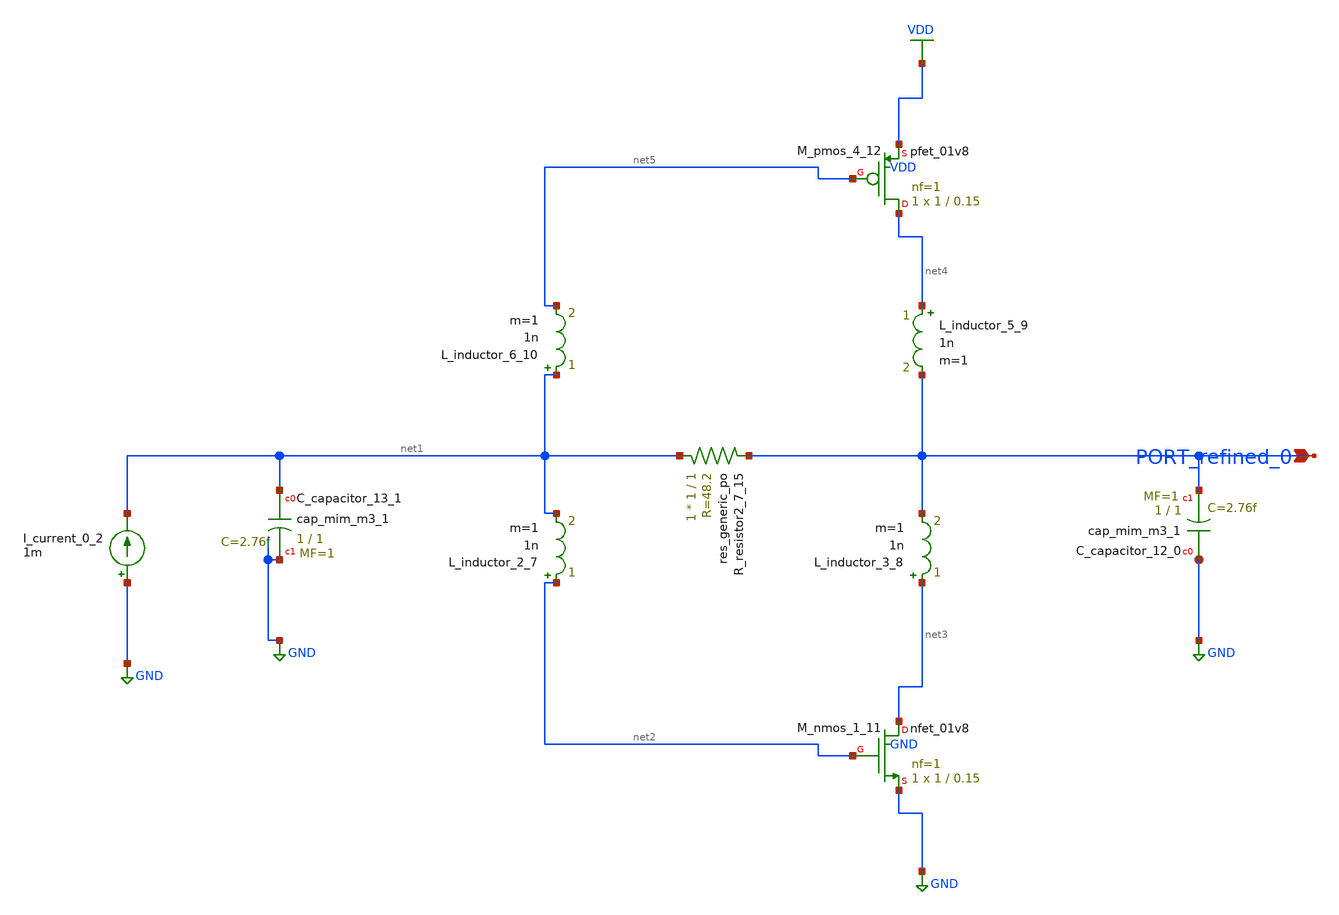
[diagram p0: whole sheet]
** sch_path: schematics/10_1109_OJCAS_2022_3164396_03_001_crop2.sch
**.subckt 10_1109_OJCAS_2022_3164396_03_001_crop2 PORT_refined_0
*.ipin PORT_refined_0
XC_capacitor_12_0 GND PORT_refined_0 sky130_fd_pr__cap_mim_m3_1 W=1 L=1 MF=1 m=1
XC_capacitor_13_1 net1 GND sky130_fd_pr__cap_mim_m3_1 W=1 L=1 MF=1 m=1
I_current_0_2 GND net1 1m
L_inductor_2_7 net2 net1 1n m=1
L_inductor_3_8 net3 PORT_refined_0 1n m=1
L_inductor_5_9 net4 PORT_refined_0 1n m=1
L_inductor_6_10 net1 net5 1n m=1
XM_nmos_1_11 net3 net2 GND GND sky130_fd_pr__nfet_01v8 L=0.15 W=1 nf=1 ad='int((1 + 1)/2) * 1 / 1 * 0.29'
+ as='int((1 + 2)/2) * 1 / 1 * 0.29' pd='2*int((1 + 1)/2) * (1 / 1 + 0.29)' ps='2*int((1 + 2)/2) * (1 / 1 + 0.29)'
+ nrd='0.29 / 1 ' nrs='0.29 / 1 ' sa=0 sb=0 sd=0 mult=1 m=1
XM_pmos_4_12 net4 net5 VDD VDD sky130_fd_pr__pfet_01v8 L=0.15 W=1 nf=1 ad='int((1 + 1)/2) * 1 / 1 * 0.29'
+ as='int((1 + 2)/2) * 1 / 1 * 0.29' pd='2*int((1 + 1)/2) * (1 / 1 + 0.29)' ps='2*int((1 + 2)/2) * (1 / 1 + 0.29)'
+ nrd='0.29 / 1 ' nrs='0.29 / 1 ' sa=0 sb=0 sd=0 mult=1 m=1
XR_resistor2_7_15 net1 PORT_refined_0 sky130_fd_pr__res_generic_po W=1 L=1 m=1
**.ends
.GLOBAL GND
.GLOBAL VDD
.end
